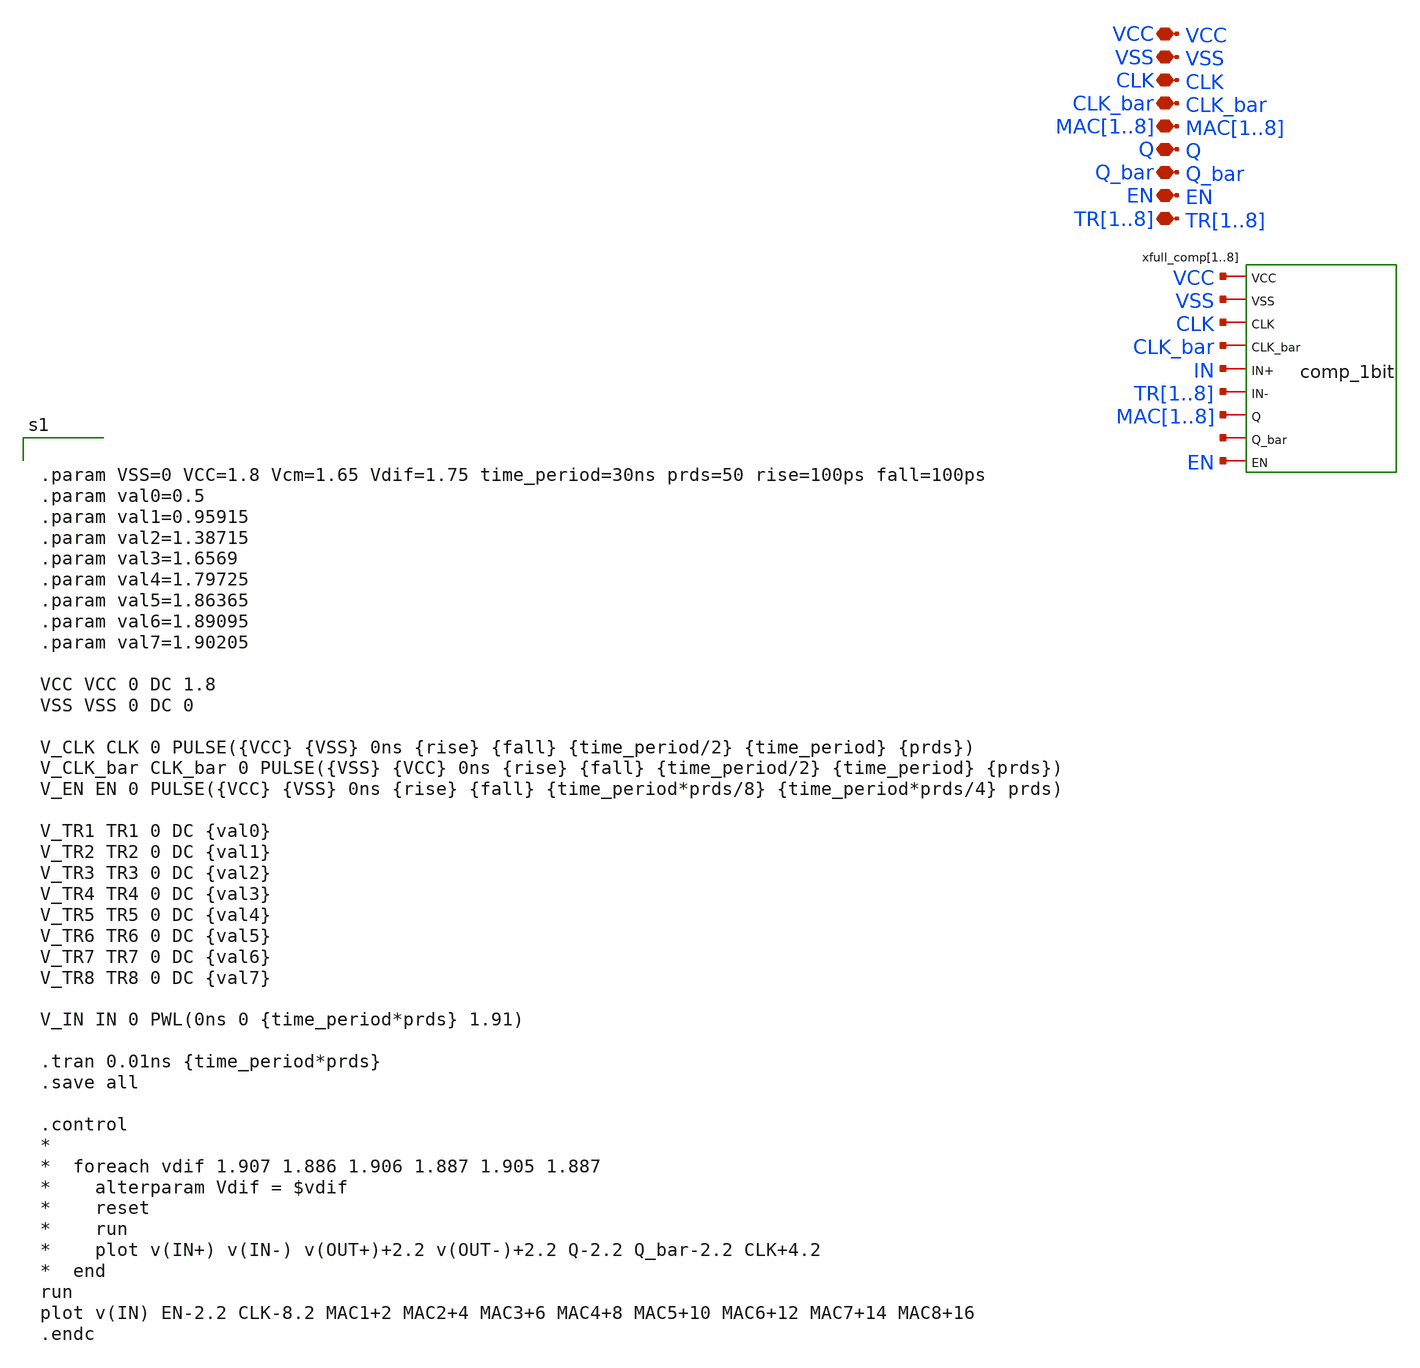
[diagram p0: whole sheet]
** sch_path: voltage_comp/comp_9_test.sch
**.subckt comp_9_test VSS VCC CLK CLK_bar Q Q_bar EN MAC1,MAC2,MAC3,MAC4,MAC5,MAC6,MAC7,MAC8
*+ TR1,TR2,TR3,TR4,TR5,TR6,TR7,TR8
*.iopin VSS
*.iopin VCC
*.iopin CLK
*.iopin CLK_bar
*.iopin Q
*.iopin Q_bar
*.iopin EN
*.iopin MAC1,MAC2,MAC3,MAC4,MAC5,MAC6,MAC7,MAC8
*.iopin TR1,TR2,TR3,TR4,TR5,TR6,TR7,TR8
xfull_comp1 VCC VSS CLK CLK_bar IN TR1 MAC1 net1[7] EN comp_1bit
xfull_comp2 VCC VSS CLK CLK_bar IN TR2 MAC2 net1[6] EN comp_1bit
xfull_comp3 VCC VSS CLK CLK_bar IN TR3 MAC3 net1[5] EN comp_1bit
xfull_comp4 VCC VSS CLK CLK_bar IN TR4 MAC4 net1[4] EN comp_1bit
xfull_comp5 VCC VSS CLK CLK_bar IN TR5 MAC5 net1[3] EN comp_1bit
xfull_comp6 VCC VSS CLK CLK_bar IN TR6 MAC6 net1[2] EN comp_1bit
xfull_comp7 VCC VSS CLK CLK_bar IN TR7 MAC7 net1[1] EN comp_1bit
xfull_comp8 VCC VSS CLK CLK_bar IN TR8 MAC8 net1[0] EN comp_1bit
**** begin user architecture code


.param VSS=0 VCC=1.8 Vcm=1.65 Vdif=1.75 time_period=30ns prds=50 rise=100ps fall=100ps
.param val0=0.5
.param val1=0.95915
.param val2=1.38715
.param val3=1.6569
.param val4=1.79725
.param val5=1.86365
.param val6=1.89095
.param val7=1.90205

VCC VCC 0 DC 1.8
VSS VSS 0 DC 0

V_CLK CLK 0 PULSE({VCC} {VSS} 0ns {rise} {fall} {time_period/2} {time_period} {prds})
V_CLK_bar CLK_bar 0 PULSE({VSS} {VCC} 0ns {rise} {fall} {time_period/2} {time_period} {prds})
V_EN EN 0 PULSE({VCC} {VSS} 0ns {rise} {fall} {time_period*prds/8} {time_period*prds/4} prds)

V_TR1 TR1 0 DC {val0}
V_TR2 TR2 0 DC {val1}
V_TR3 TR3 0 DC {val2}
V_TR4 TR4 0 DC {val3}
V_TR5 TR5 0 DC {val4}
V_TR6 TR6 0 DC {val5}
V_TR7 TR7 0 DC {val6}
V_TR8 TR8 0 DC {val7}

V_IN IN 0 PWL(0ns 0 {time_period*prds} 1.91)

.tran 0.01ns {time_period*prds}
.save all

.control
*
*  foreach vdif 1.907 1.886 1.906 1.887 1.905 1.887
*    alterparam Vdif = $vdif
*    reset
*    run
*    plot v(IN+) v(IN-) v(OUT+)+2.2 v(OUT-)+2.2 Q-2.2 Q_bar-2.2 CLK+4.2
*  end
run
plot v(IN) EN-2.2 CLK-8.2 MAC1+2 MAC2+4 MAC3+6 MAC4+8 MAC5+10 MAC6+12 MAC7+14 MAC8+16
.endc



** opencircuitdesign pdks install
.lib $::SKYWATER_MODELS/sky130.lib.spice tt

**** end user architecture code
**.ends
.end
